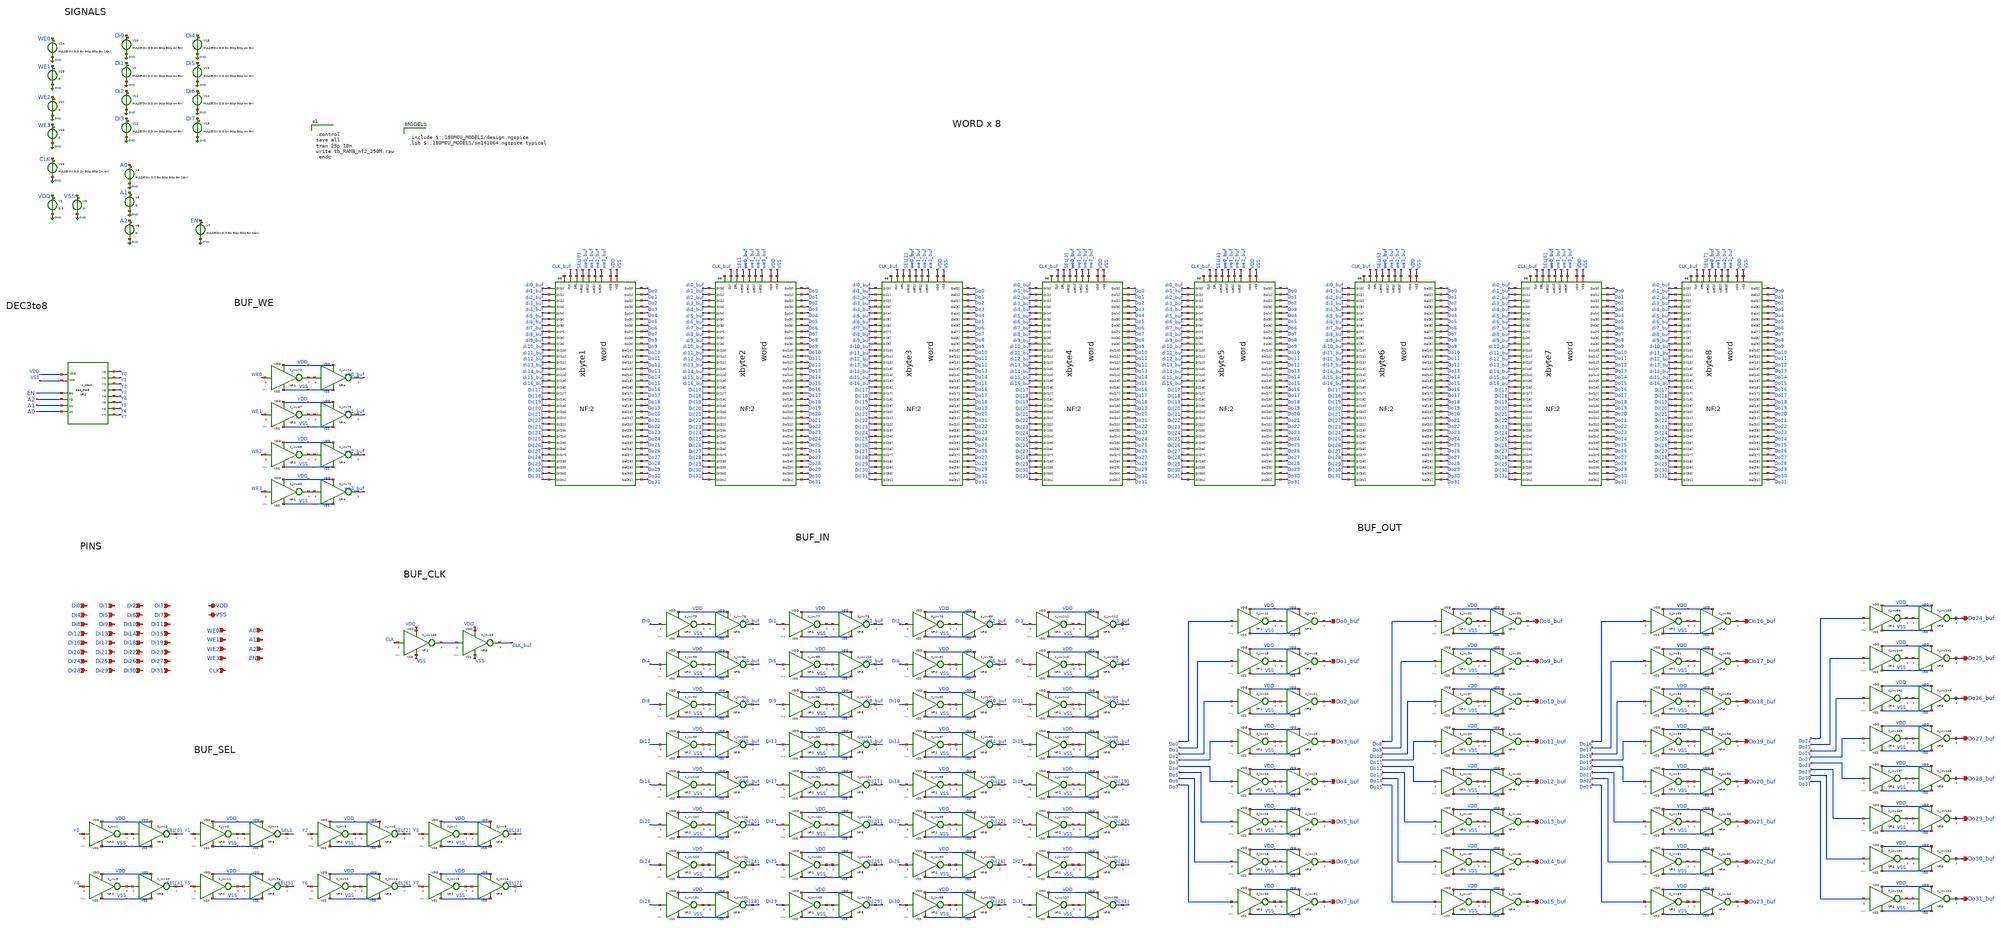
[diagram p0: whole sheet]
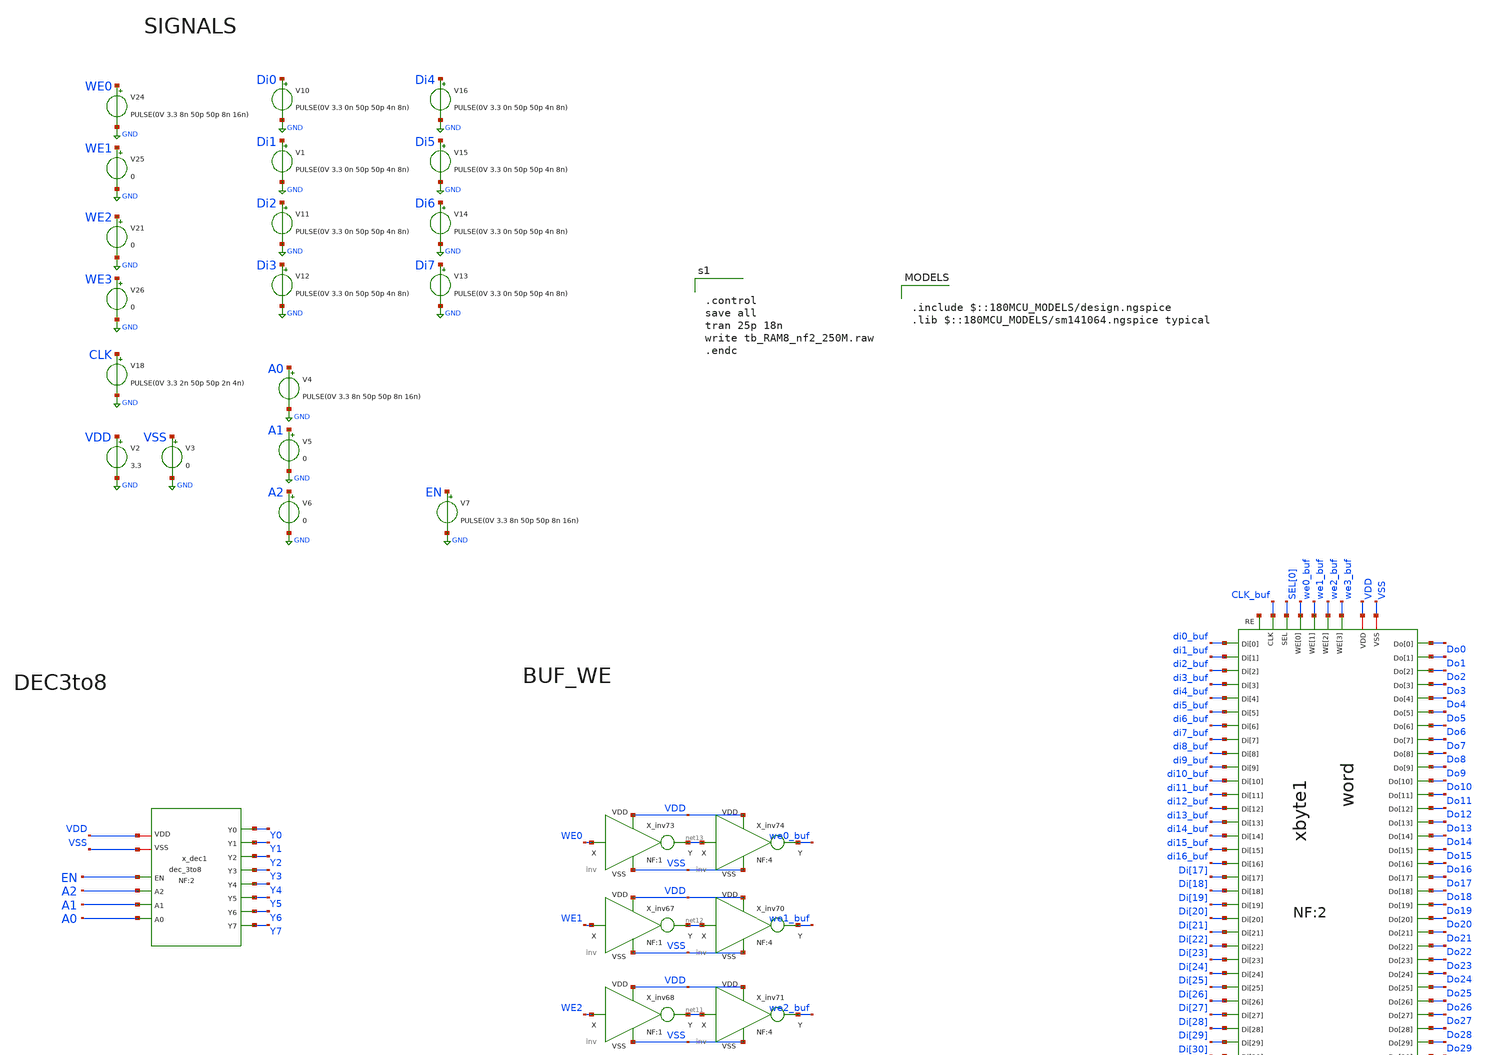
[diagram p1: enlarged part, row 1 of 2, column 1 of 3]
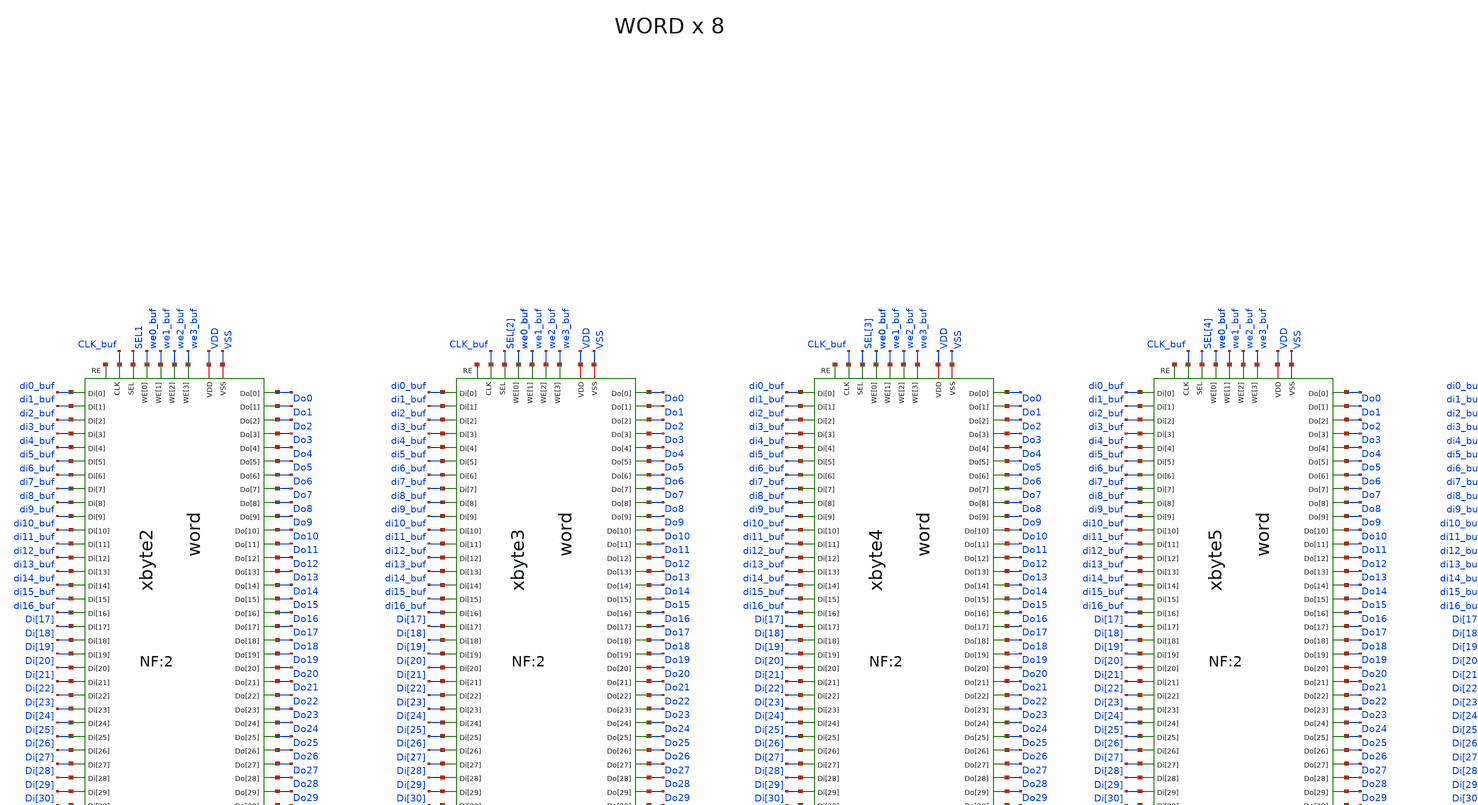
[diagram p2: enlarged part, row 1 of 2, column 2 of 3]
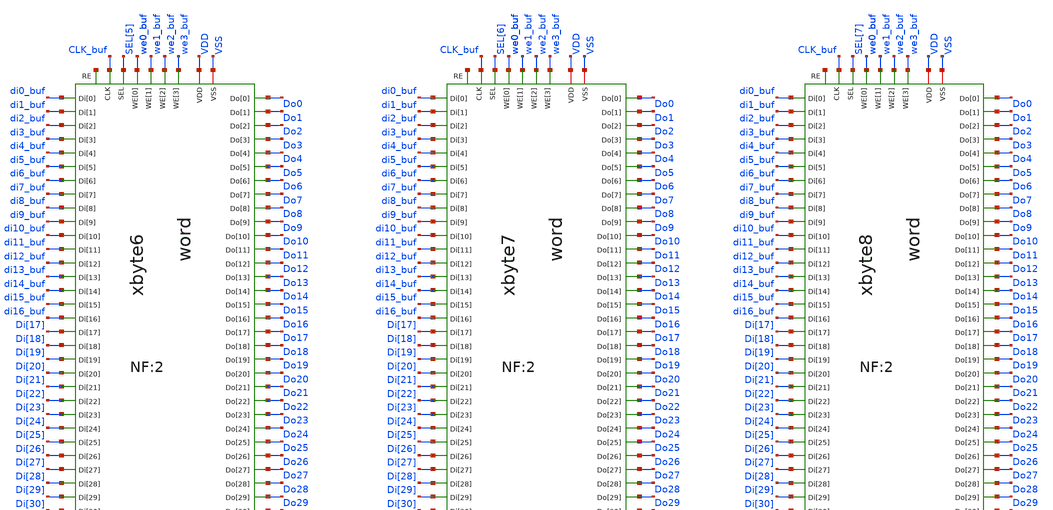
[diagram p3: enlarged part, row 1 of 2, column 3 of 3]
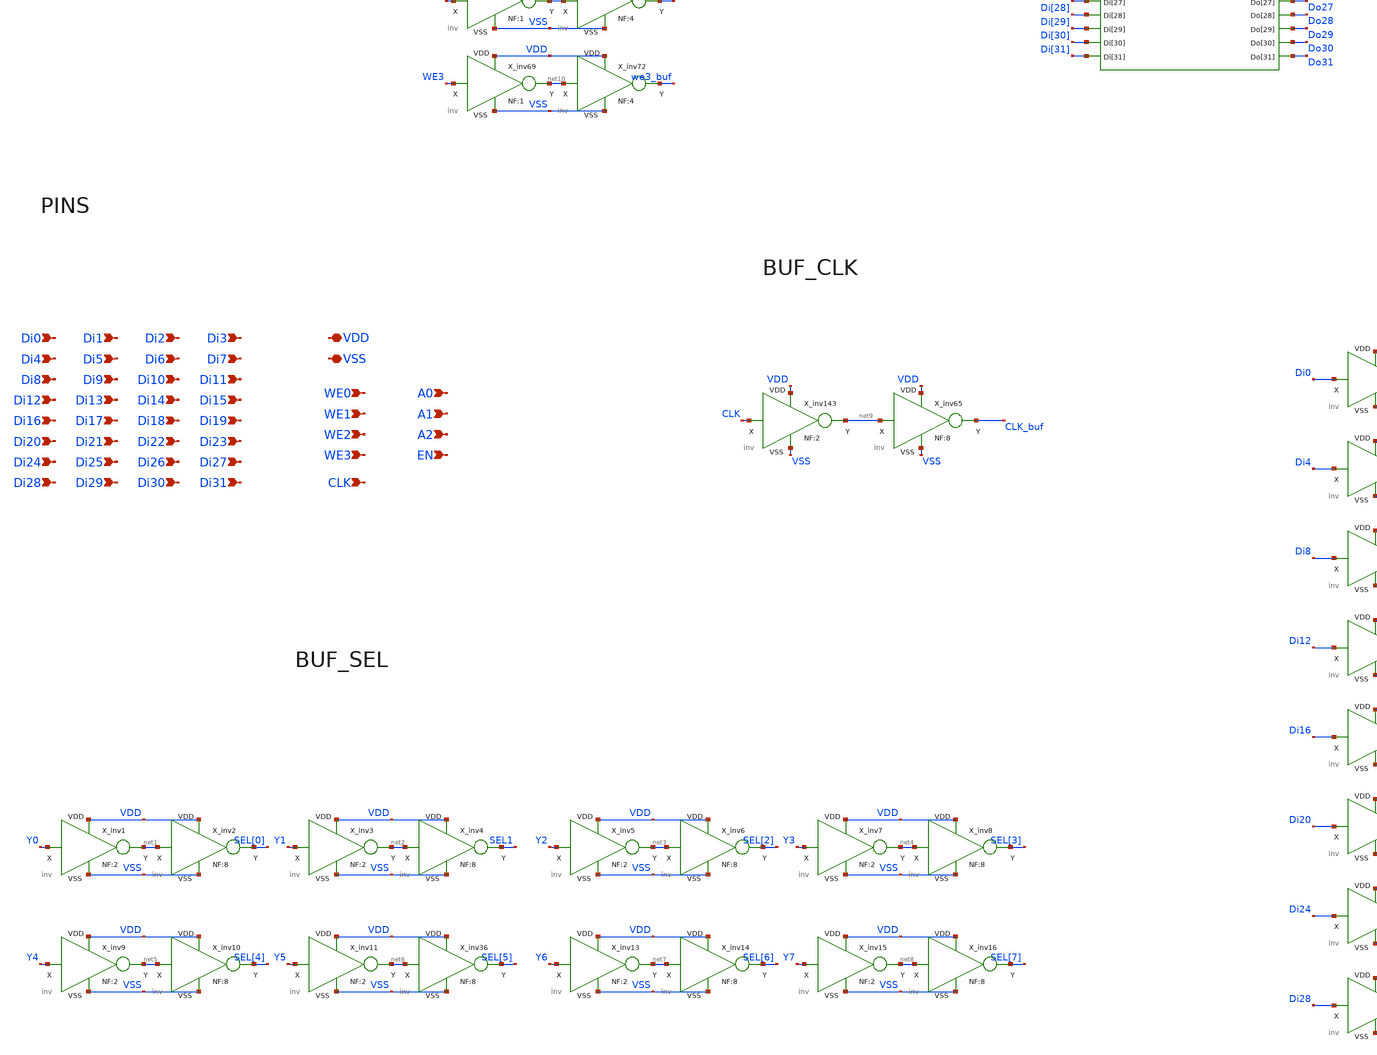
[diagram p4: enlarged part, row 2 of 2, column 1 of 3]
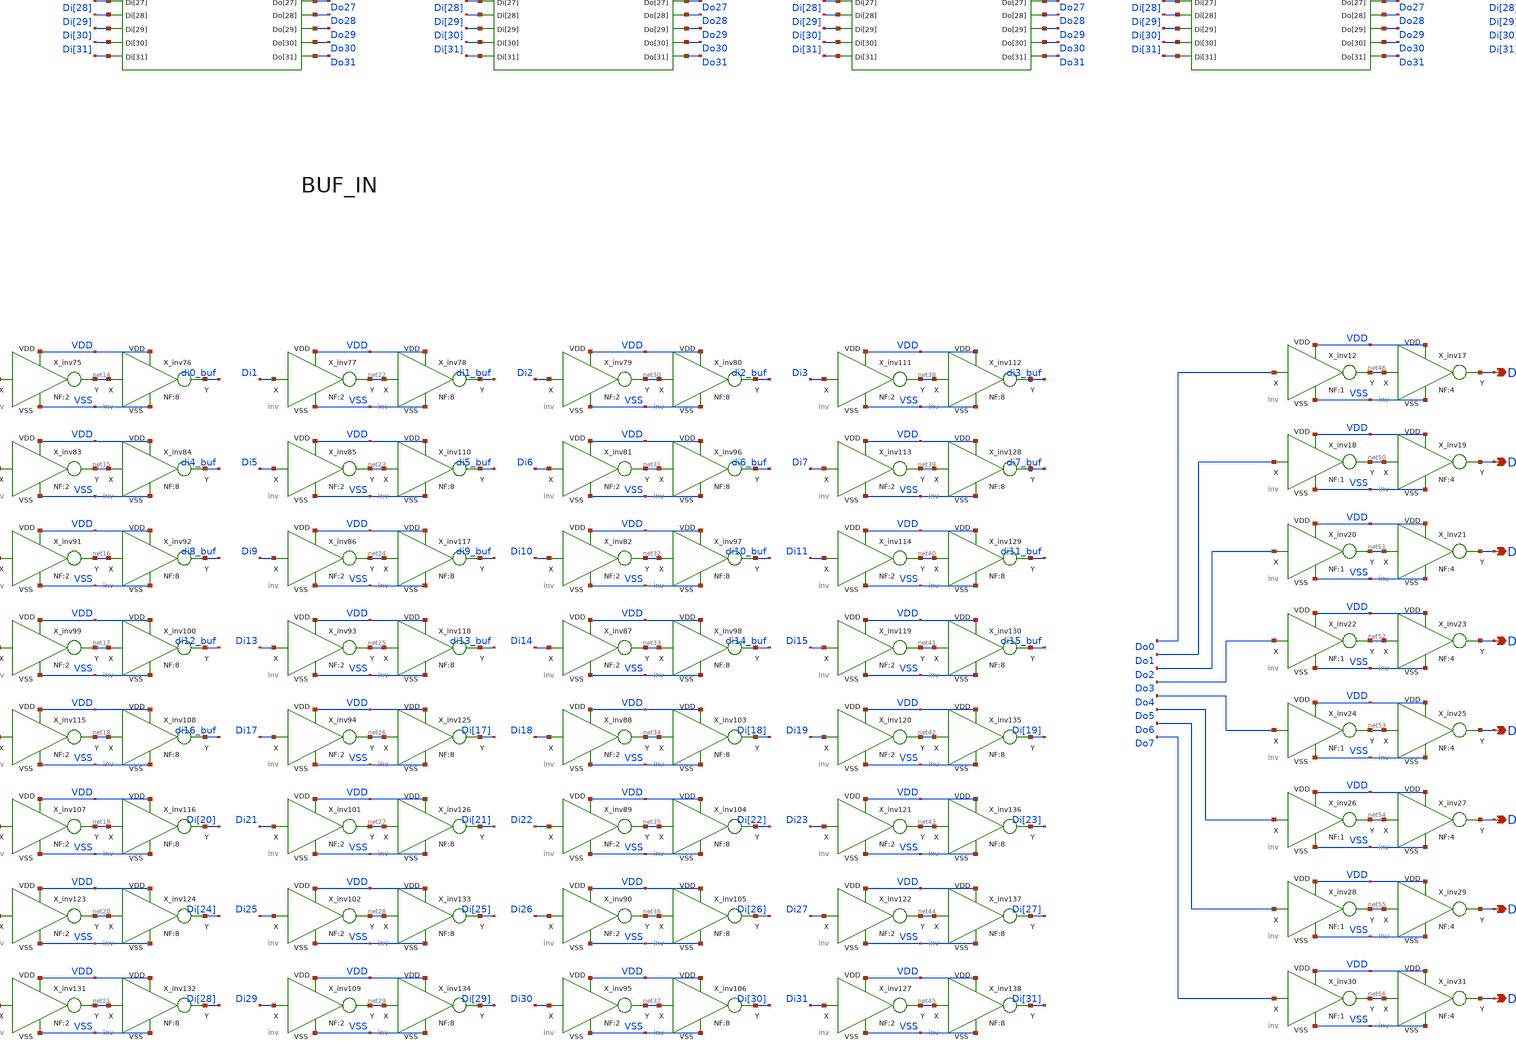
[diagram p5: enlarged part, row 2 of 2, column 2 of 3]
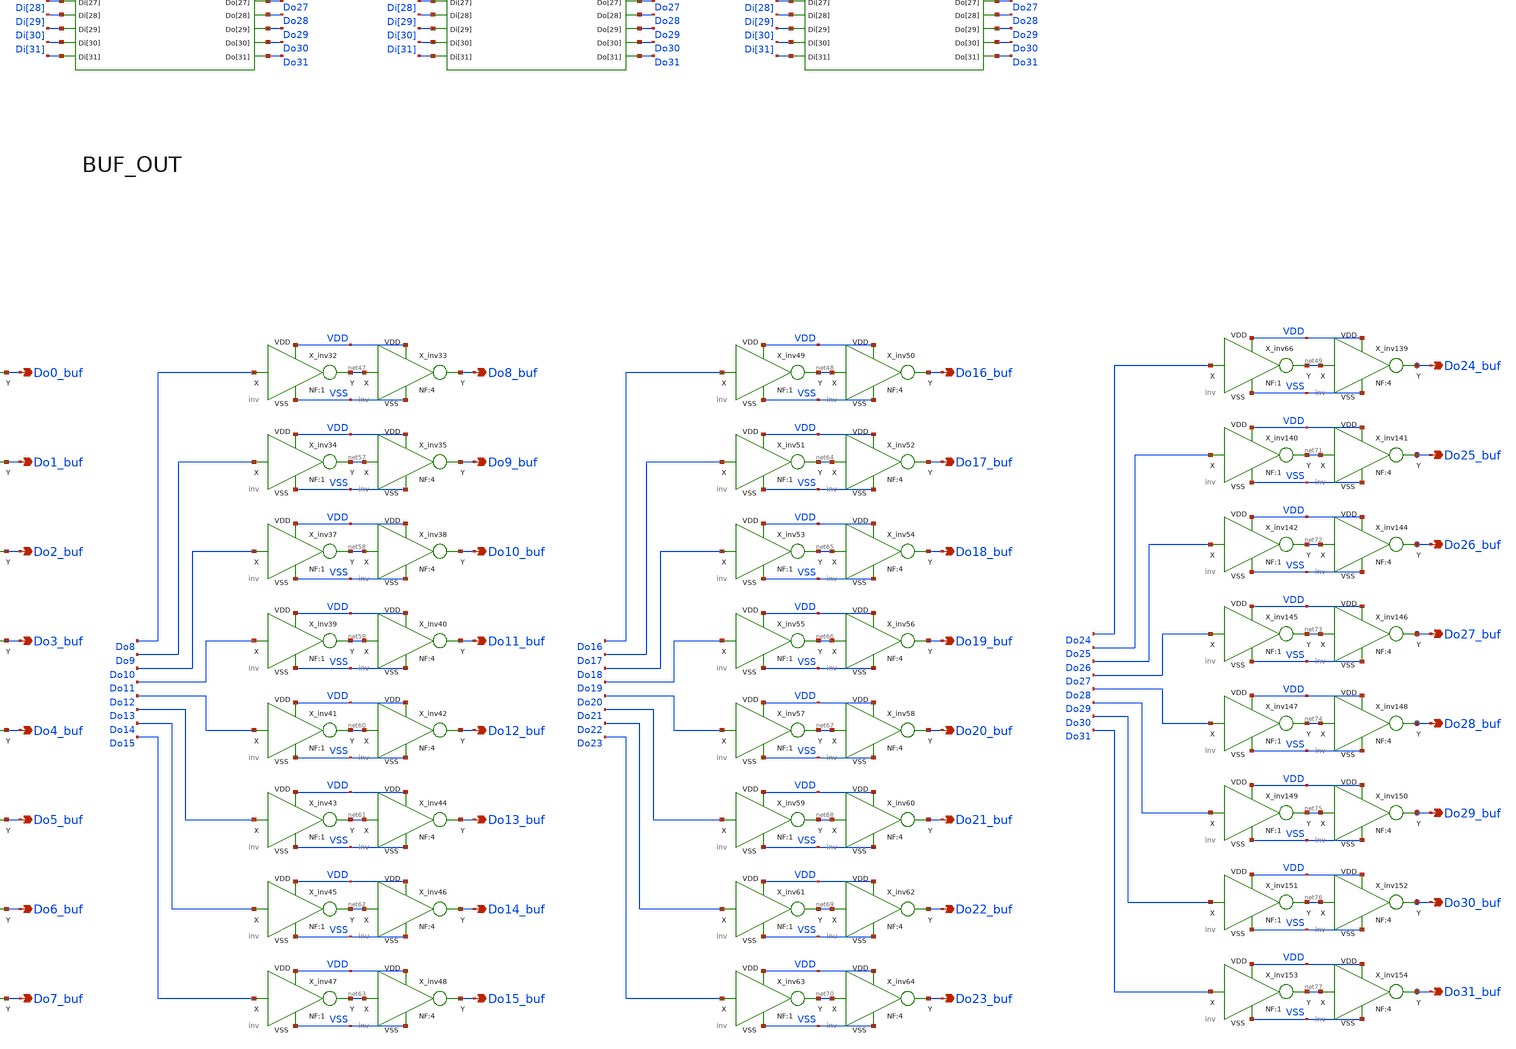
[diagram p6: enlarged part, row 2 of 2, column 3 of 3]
** sch_path: xschem_lib/DFFRAM_full_custom/tb_RAM8.sch
**.subckt tb_RAM8 Di0 Do0_buf Di1 Do1_buf Di2 Do2_buf Di3 Do3_buf Di4 Do4_buf Di5 Do5_buf Di6
*+ Do6_buf Di7 Do7_buf Di8 Do8_buf Di9 Do9_buf Di10 Do10_buf Di11 Do11_buf Di12 Do12_buf Di13 Do13_buf Di14
*+ Do14_buf Di15 Do15_buf Di16 Do16_buf Di17 Do17_buf Di18 Do18_buf Di19 Do19_buf Di20 Do20_buf Di21 Do21_buf
*+ Di22 Do22_buf Di23 Do23_buf Di24 Do24_buf Di25 Do25_buf Di26 Do26_buf Di27 Do27_buf Di28 Do28_buf Di29
*+ Do29_buf Di30 Do30_buf Di31 Do31_buf VDD VSS WE0 WE1 WE2 WE3 CLK A0 A1 A2 EN
*.ipin Di0
*.opin Do0_buf
*.ipin Di1
*.opin Do1_buf
*.ipin Di2
*.opin Do2_buf
*.ipin Di3
*.opin Do3_buf
*.ipin Di4
*.opin Do4_buf
*.ipin Di5
*.opin Do5_buf
*.ipin Di6
*.opin Do6_buf
*.ipin Di7
*.opin Do7_buf
*.ipin Di8
*.opin Do8_buf
*.ipin Di9
*.opin Do9_buf
*.ipin Di10
*.opin Do10_buf
*.ipin Di11
*.opin Do11_buf
*.ipin Di12
*.opin Do12_buf
*.ipin Di13
*.opin Do13_buf
*.ipin Di14
*.opin Do14_buf
*.ipin Di15
*.opin Do15_buf
*.ipin Di16
*.opin Do16_buf
*.ipin Di17
*.opin Do17_buf
*.ipin Di18
*.opin Do18_buf
*.ipin Di19
*.opin Do19_buf
*.ipin Di20
*.opin Do20_buf
*.ipin Di21
*.opin Do21_buf
*.ipin Di22
*.opin Do22_buf
*.ipin Di23
*.opin Do23_buf
*.ipin Di24
*.opin Do24_buf
*.ipin Di25
*.opin Do25_buf
*.ipin Di26
*.opin Do26_buf
*.ipin Di27
*.opin Do27_buf
*.ipin Di28
*.opin Do28_buf
*.ipin Di29
*.opin Do29_buf
*.ipin Di30
*.opin Do30_buf
*.ipin Di31
*.opin Do31_buf
*.iopin VDD
*.iopin VSS
*.ipin WE0
*.ipin WE1
*.ipin WE2
*.ipin WE3
*.ipin CLK
*.ipin A0
*.ipin A1
*.ipin A2
*.ipin EN
xbyte1 VDD VSS we3_buf we2_buf we1_buf we0_buf SEL[0] CLK_buf di9_buf di7_buf Di[19] Di[20] Di[30]
+ di8_buf di10_buf di4_buf di12_buf Di[24] di5_buf Di[23] Di[29] di3_buf di14_buf Di[18] Di[28] Di[17]
+ di16_buf Di[27] Di[21] Di[22] di0_buf di1_buf Di[31] Di[26] Di[25] di15_buf di2_buf di13_buf di6_buf
+ di11_buf Do21 Do22 Do27 Do23 Do28 Do8 Do9 Do10 Do11 Do12 Do29 Do30 Do13 Do14 Do15 Do16 Do24 Do17 Do1 Do7 Do6
+ Do5 Do18 Do0 Do2 Do3 Do4 Do19 Do20 Do25 Do26 Do31 net78 word NF=2
xbyte2 VDD VSS we3_buf we2_buf we1_buf we0_buf SEL1 CLK_buf di9_buf di7_buf Di[19] Di[20] Di[30]
+ di8_buf di10_buf di4_buf di12_buf Di[24] di5_buf Di[23] Di[29] di3_buf di14_buf Di[18] Di[28] Di[17]
+ di16_buf Di[27] Di[21] Di[22] di0_buf di1_buf Di[31] Di[26] Di[25] di15_buf di2_buf di13_buf di6_buf
+ di11_buf Do21 Do22 Do27 Do23 Do28 Do8 Do9 Do10 Do11 Do12 Do29 Do30 Do13 Do14 Do15 Do16 Do24 Do17 Do1 Do7 Do6
+ Do5 Do18 Do0 Do2 Do3 Do4 Do19 Do20 Do25 Do26 Do31 net79 word NF=2
xbyte3 VDD VSS we3_buf we2_buf we1_buf we0_buf SEL[2] CLK_buf di9_buf di7_buf Di[19] Di[20] Di[30]
+ di8_buf di10_buf di4_buf di12_buf Di[24] di5_buf Di[23] Di[29] di3_buf di14_buf Di[18] Di[28] Di[17]
+ di16_buf Di[27] Di[21] Di[22] di0_buf di1_buf Di[31] Di[26] Di[25] di15_buf di2_buf di13_buf di6_buf
+ di11_buf Do21 Do22 Do27 Do23 Do28 Do8 Do9 Do10 Do11 Do12 Do29 Do30 Do13 Do14 Do15 Do16 Do24 Do17 Do1 Do7 Do6
+ Do5 Do18 Do0 Do2 Do3 Do4 Do19 Do20 Do25 Do26 Do31 net80 word NF=2
xbyte4 VDD VSS we3_buf we2_buf we1_buf we0_buf SEL[3] CLK_buf di9_buf di7_buf Di[19] Di[20] Di[30]
+ di8_buf di10_buf di4_buf di12_buf Di[24] di5_buf Di[23] Di[29] di3_buf di14_buf Di[18] Di[28] Di[17]
+ di16_buf Di[27] Di[21] Di[22] di0_buf di1_buf Di[31] Di[26] Di[25] di15_buf di2_buf di13_buf di6_buf
+ di11_buf Do21 Do22 Do27 Do23 Do28 Do8 Do9 Do10 Do11 Do12 Do29 Do30 Do13 Do14 Do15 Do16 Do24 Do17 Do1 Do7 Do6
+ Do5 Do18 Do0 Do2 Do3 Do4 Do19 Do20 Do25 Do26 Do31 net81 word NF=2
xbyte5 VDD VSS we3_buf we2_buf we1_buf we0_buf SEL[4] CLK_buf di9_buf di7_buf Di[19] Di[20] Di[30]
+ di8_buf di10_buf di4_buf di12_buf Di[24] di5_buf Di[23] Di[29] di3_buf di14_buf Di[18] Di[28] Di[17]
+ di16_buf Di[27] Di[21] Di[22] di0_buf di1_buf Di[31] Di[26] Di[25] di15_buf di2_buf di13_buf di6_buf
+ di11_buf Do21 Do22 Do27 Do23 Do28 Do8 Do9 Do10 Do11 Do12 Do29 Do30 Do13 Do14 Do15 Do16 Do24 Do17 Do1 Do7 Do6
+ Do5 Do18 Do0 Do2 Do3 Do4 Do19 Do20 Do25 Do26 Do31 net82 word NF=2
xbyte6 VDD VSS we3_buf we2_buf we1_buf we0_buf SEL[5] CLK_buf di9_buf di7_buf Di[19] Di[20] Di[30]
+ di8_buf di10_buf di4_buf di12_buf Di[24] di5_buf Di[23] Di[29] di3_buf di14_buf Di[18] Di[28] Di[17]
+ di16_buf Di[27] Di[21] Di[22] di0_buf di1_buf Di[31] Di[26] Di[25] di15_buf di2_buf di13_buf di6_buf
+ di11_buf Do21 Do22 Do27 Do23 Do28 Do8 Do9 Do10 Do11 Do12 Do29 Do30 Do13 Do14 Do15 Do16 Do24 Do17 Do1 Do7 Do6
+ Do5 Do18 Do0 Do2 Do3 Do4 Do19 Do20 Do25 Do26 Do31 net83 word NF=2
xbyte7 VDD VSS we3_buf we2_buf we1_buf we0_buf SEL[6] CLK_buf di9_buf di7_buf Di[19] Di[20] Di[30]
+ di8_buf di10_buf di4_buf di12_buf Di[24] di5_buf Di[23] Di[29] di3_buf di14_buf Di[18] Di[28] Di[17]
+ di16_buf Di[27] Di[21] Di[22] di0_buf di1_buf Di[31] Di[26] Di[25] di15_buf di2_buf di13_buf di6_buf
+ di11_buf Do21 Do22 Do27 Do23 Do28 Do8 Do9 Do10 Do11 Do12 Do29 Do30 Do13 Do14 Do15 Do16 Do24 Do17 Do1 Do7 Do6
+ Do5 Do18 Do0 Do2 Do3 Do4 Do19 Do20 Do25 Do26 Do31 net84 word NF=2
xbyte8 VDD VSS we3_buf we2_buf we1_buf we0_buf SEL[7] CLK_buf di9_buf di7_buf Di[19] Di[20] Di[30]
+ di8_buf di10_buf di4_buf di12_buf Di[24] di5_buf Di[23] Di[29] di3_buf di14_buf Di[18] Di[28] Di[17]
+ di16_buf Di[27] Di[21] Di[22] di0_buf di1_buf Di[31] Di[26] Di[25] di15_buf di2_buf di13_buf di6_buf
+ di11_buf Do21 Do22 Do27 Do23 Do28 Do8 Do9 Do10 Do11 Do12 Do29 Do30 Do13 Do14 Do15 Do16 Do24 Do17 Do1 Do7 Do6
+ Do5 Do18 Do0 Do2 Do3 Do4 Do19 Do20 Do25 Do26 Do31 net85 word NF=2
x_dec1 A1 EN A2 A0 VDD VSS Y0 Y1 Y2 Y3 Y4 Y5 Y6 Y7 dec_3to8 NF=2
X_inv1 Y0 VDD VSS net1 inv NF=2
X_inv2 net1 VDD VSS SEL[0] inv NF=8
X_inv3 Y1 VDD VSS net2 inv NF=2
X_inv4 net2 VDD VSS SEL1 inv NF=8
X_inv65 net9 VDD VSS CLK_buf inv NF=8
X_inv73 WE0 VDD VSS net13 inv NF=1
X_inv74 net13 VDD VSS we0_buf inv NF=4
X_inv75 Di0 VDD VSS net14 inv NF=2
X_inv76 net14 VDD VSS di0_buf inv NF=8
X_inv143 CLK VDD VSS net9 inv NF=2
X_inv9 Y4 VDD VSS net5 inv NF=2
X_inv10 net5 VDD VSS SEL[4] inv NF=8
X_inv11 Y5 VDD VSS net6 inv NF=2
X_inv36 net6 VDD VSS SEL[5] inv NF=8
X_inv5 Y2 VDD VSS net3 inv NF=2
X_inv13 Y6 VDD VSS net7 inv NF=2
X_inv6 net3 VDD VSS SEL[2] inv NF=8
X_inv14 net7 VDD VSS SEL[6] inv NF=8
X_inv7 Y3 VDD VSS net4 inv NF=2
X_inv15 Y7 VDD VSS net8 inv NF=2
X_inv8 net4 VDD VSS SEL[3] inv NF=8
X_inv16 net8 VDD VSS SEL[7] inv NF=8
X_inv67 WE1 VDD VSS net12 inv NF=1
X_inv68 WE2 VDD VSS net11 inv NF=1
X_inv69 WE3 VDD VSS net10 inv NF=1
X_inv70 net12 VDD VSS we1_buf inv NF=4
X_inv71 net11 VDD VSS we2_buf inv NF=4
X_inv72 net10 VDD VSS we3_buf inv NF=4
X_inv12 Do0 VDD VSS net46 inv NF=1
X_inv17 net46 VDD VSS Do0_buf inv NF=4
X_inv32 Do8 VDD VSS net47 inv NF=1
X_inv33 net47 VDD VSS Do8_buf inv NF=4
X_inv49 Do16 VDD VSS net48 inv NF=1
X_inv50 net48 VDD VSS Do16_buf inv NF=4
X_inv66 Do24 VDD VSS net49 inv NF=1
X_inv139 net49 VDD VSS Do24_buf inv NF=4
X_inv18 Do1 VDD VSS net50 inv NF=1
X_inv19 net50 VDD VSS Do1_buf inv NF=4
X_inv20 Do2 VDD VSS net51 inv NF=1
X_inv21 net51 VDD VSS Do2_buf inv NF=4
X_inv22 Do3 VDD VSS net52 inv NF=1
X_inv23 net52 VDD VSS Do3_buf inv NF=4
X_inv24 Do4 VDD VSS net53 inv NF=1
X_inv25 net53 VDD VSS Do4_buf inv NF=4
X_inv26 Do5 VDD VSS net54 inv NF=1
X_inv27 net54 VDD VSS Do5_buf inv NF=4
X_inv28 Do6 VDD VSS net55 inv NF=1
X_inv29 net55 VDD VSS Do6_buf inv NF=4
X_inv30 Do7 VDD VSS net56 inv NF=1
X_inv31 net56 VDD VSS Do7_buf inv NF=4
X_inv34 Do9 VDD VSS net57 inv NF=1
X_inv35 net57 VDD VSS Do9_buf inv NF=4
X_inv37 Do10 VDD VSS net58 inv NF=1
X_inv38 net58 VDD VSS Do10_buf inv NF=4
X_inv39 Do11 VDD VSS net59 inv NF=1
X_inv40 net59 VDD VSS Do11_buf inv NF=4
X_inv41 Do12 VDD VSS net60 inv NF=1
X_inv42 net60 VDD VSS Do12_buf inv NF=4
X_inv43 Do13 VDD VSS net61 inv NF=1
X_inv44 net61 VDD VSS Do13_buf inv NF=4
X_inv45 Do14 VDD VSS net62 inv NF=1
X_inv46 net62 VDD VSS Do14_buf inv NF=4
X_inv47 Do15 VDD VSS net63 inv NF=1
X_inv48 net63 VDD VSS Do15_buf inv NF=4
X_inv51 Do17 VDD VSS net64 inv NF=1
X_inv52 net64 VDD VSS Do17_buf inv NF=4
X_inv53 Do18 VDD VSS net65 inv NF=1
X_inv54 net65 VDD VSS Do18_buf inv NF=4
X_inv55 Do19 VDD VSS net66 inv NF=1
X_inv56 net66 VDD VSS Do19_buf inv NF=4
X_inv57 Do20 VDD VSS net67 inv NF=1
X_inv58 net67 VDD VSS Do20_buf inv NF=4
X_inv59 Do21 VDD VSS net68 inv NF=1
X_inv60 net68 VDD VSS Do21_buf inv NF=4
X_inv61 Do22 VDD VSS net69 inv NF=1
X_inv62 net69 VDD VSS Do22_buf inv NF=4
X_inv63 Do23 VDD VSS net70 inv NF=1
X_inv64 net70 VDD VSS Do23_buf inv NF=4
X_inv140 Do25 VDD VSS net71 inv NF=1
X_inv141 net71 VDD VSS Do25_buf inv NF=4
X_inv142 Do26 VDD VSS net72 inv NF=1
X_inv144 net72 VDD VSS Do26_buf inv NF=4
X_inv145 Do27 VDD VSS net73 inv NF=1
X_inv146 net73 VDD VSS Do27_buf inv NF=4
X_inv147 Do28 VDD VSS net74 inv NF=1
X_inv148 net74 VDD VSS Do28_buf inv NF=4
X_inv149 Do29 VDD VSS net75 inv NF=1
X_inv150 net75 VDD VSS Do29_buf inv NF=4
X_inv151 Do30 VDD VSS net76 inv NF=1
X_inv152 net76 VDD VSS Do30_buf inv NF=4
X_inv153 Do31 VDD VSS net77 inv NF=1
X_inv154 net77 VDD VSS Do31_buf inv NF=4
X_inv83 Di4 VDD VSS net15 inv NF=2
X_inv91 Di8 VDD VSS net16 inv NF=2
X_inv99 Di12 VDD VSS net17 inv NF=2
X_inv115 Di16 VDD VSS net18 inv NF=2
X_inv107 Di20 VDD VSS net19 inv NF=2
X_inv123 Di24 VDD VSS net20 inv NF=2
X_inv131 Di28 VDD VSS net21 inv NF=2
X_inv77 Di1 VDD VSS net22 inv NF=2
X_inv85 Di5 VDD VSS net23 inv NF=2
X_inv86 Di9 VDD VSS net24 inv NF=2
X_inv93 Di13 VDD VSS net25 inv NF=2
X_inv94 Di17 VDD VSS net26 inv NF=2
X_inv101 Di21 VDD VSS net27 inv NF=2
X_inv102 Di25 VDD VSS net28 inv NF=2
X_inv109 Di29 VDD VSS net29 inv NF=2
X_inv84 net15 VDD VSS di4_buf inv NF=8
X_inv92 net16 VDD VSS di8_buf inv NF=8
X_inv100 net17 VDD VSS di12_buf inv NF=8
X_inv108 net18 VDD VSS di16_buf inv NF=8
X_inv116 net19 VDD VSS Di[20] inv NF=8
X_inv124 net20 VDD VSS Di[24] inv NF=8
X_inv132 net21 VDD VSS Di[28] inv NF=8
X_inv78 net22 VDD VSS di1_buf inv NF=8
X_inv110 net23 VDD VSS di5_buf inv NF=8
X_inv117 net24 VDD VSS di9_buf inv NF=8
X_inv118 net25 VDD VSS di13_buf inv NF=8
X_inv125 net26 VDD VSS Di[17] inv NF=8
X_inv126 net27 VDD VSS Di[21] inv NF=8
X_inv133 net28 VDD VSS Di[25] inv NF=8
X_inv134 net29 VDD VSS Di[29] inv NF=8
X_inv80 net30 VDD VSS di2_buf inv NF=8
X_inv96 net31 VDD VSS di6_buf inv NF=8
X_inv97 net32 VDD VSS di10_buf inv NF=8
X_inv98 net33 VDD VSS di14_buf inv NF=8
X_inv103 net34 VDD VSS Di[18] inv NF=8
X_inv104 net35 VDD VSS Di[22] inv NF=8
X_inv105 net36 VDD VSS Di[26] inv NF=8
X_inv106 net37 VDD VSS Di[30] inv NF=8
X_inv112 net38 VDD VSS di3_buf inv NF=8
X_inv128 net39 VDD VSS di7_buf inv NF=8
X_inv129 net40 VDD VSS di11_buf inv NF=8
X_inv130 net41 VDD VSS di15_buf inv NF=8
X_inv135 net42 VDD VSS Di[19] inv NF=8
X_inv136 net43 VDD VSS Di[23] inv NF=8
X_inv137 net44 VDD VSS Di[27] inv NF=8
X_inv138 net45 VDD VSS Di[31] inv NF=8
X_inv79 Di2 VDD VSS net30 inv NF=2
X_inv81 Di6 VDD VSS net31 inv NF=2
X_inv82 Di10 VDD VSS net32 inv NF=2
X_inv87 Di14 VDD VSS net33 inv NF=2
X_inv88 Di18 VDD VSS net34 inv NF=2
X_inv89 Di22 VDD VSS net35 inv NF=2
X_inv90 Di26 VDD VSS net36 inv NF=2
X_inv95 Di30 VDD VSS net37 inv NF=2
X_inv111 Di3 VDD VSS net38 inv NF=2
X_inv113 Di7 VDD VSS net39 inv NF=2
X_inv114 Di11 VDD VSS net40 inv NF=2
X_inv119 Di15 VDD VSS net41 inv NF=2
X_inv120 Di19 VDD VSS net42 inv NF=2
X_inv121 Di23 VDD VSS net43 inv NF=2
X_inv122 Di27 VDD VSS net44 inv NF=2
X_inv127 Di31 VDD VSS net45 inv NF=2
V2 VDD GND 3.3
V3 VSS GND 0
V18 CLK GND PULSE(0V 3.3 2n 50p 50p 2n 4n)
V10 Di0 GND PULSE(0V 3.3 0n 50p 50p 4n 8n)
V4 A0 GND PULSE(0V 3.3 8n 50p 50p 8n 16n)
V5 A1 GND 0
V6 A2 GND 0
V1 Di1 GND PULSE(0V 3.3 0n 50p 50p 4n 8n)
V11 Di2 GND PULSE(0V 3.3 0n 50p 50p 4n 8n)
V12 Di3 GND PULSE(0V 3.3 0n 50p 50p 4n 8n)
V13 Di7 GND PULSE(0V 3.3 0n 50p 50p 4n 8n)
V14 Di6 GND PULSE(0V 3.3 0n 50p 50p 4n 8n)
V15 Di5 GND PULSE(0V 3.3 0n 50p 50p 4n 8n)
V16 Di4 GND PULSE(0V 3.3 0n 50p 50p 4n 8n)
V7 EN GND PULSE(0V 3.3 8n 50p 50p 8n 16n)
V24 WE0 GND PULSE(0V 3.3 8n 50p 50p 8n 16n)
V25 WE1 GND 0
V26 WE3 GND 0
V21 WE2 GND 0
**** begin user architecture code


.control
save all
tran 25p 18n
write tb_RAM8_nf2_250M.raw
.endc



.include $::180MCU_MODELS/design.ngspice
.lib $::180MCU_MODELS/sm141064.ngspice typical

**** end user architecture code
**.ends
.GLOBAL GND
.end
